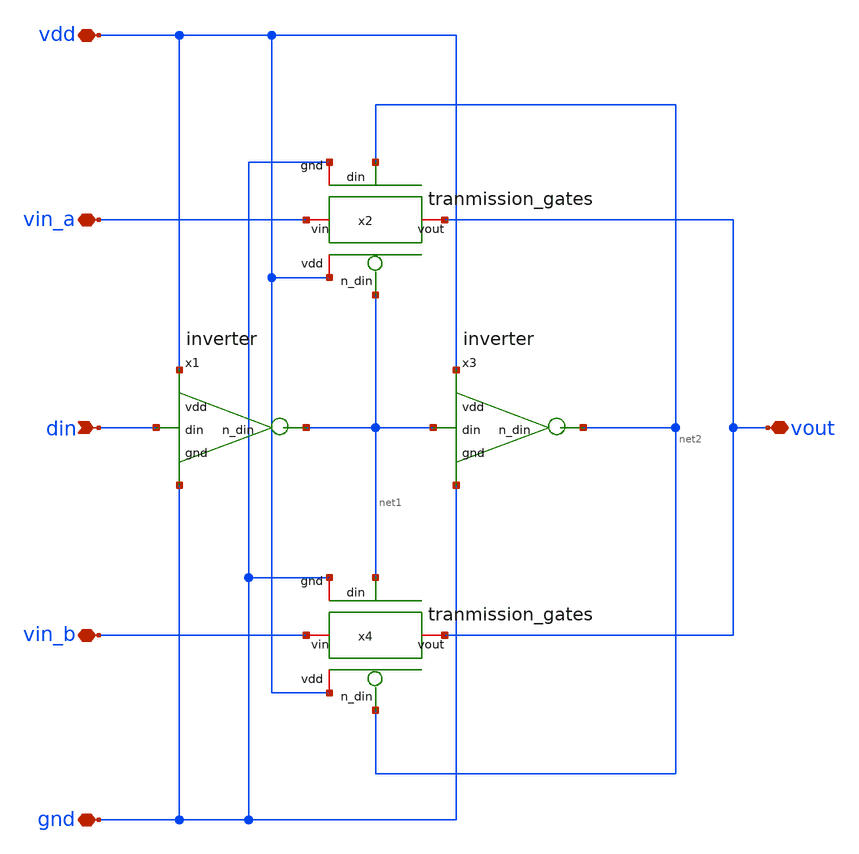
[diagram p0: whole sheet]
** sch_path: Symbols/spdt_sw.sch
**.subckt spdt_sw vdd gnd vout vin_a vin_b din
*.iopin vdd
*.iopin gnd
*.iopin vout
*.iopin vin_a
*.iopin vin_b
*.ipin din
x1 vdd din net1 gnd inverter
x2 net1 vdd vout vin_a gnd net2 tranmission_gates
x3 vdd net1 net2 gnd inverter
x4 net2 vdd vout vin_b gnd net1 tranmission_gates
**.ends

* expanding   symbol:  inverter.sym # of pins=4
** sym_path: Symbols/inverter.sym
** sch_path: Symbols/inverter.sch
.subckt inverter vdd din n_din gnd
*.ipin gnd
*.opin n_din
*.ipin din
*.ipin vdd
XM3 n_din din vdd vdd sky130_fd_pr__pfet_01v8 L=1 W=1 nf=1 ad='int((nf+1)/2) * W/nf * 0.29' as='int((nf+2)/2) * W/nf * 0.29'
+ pd='2*int((nf+1)/2) * (W/nf + 0.29)' ps='2*int((nf+2)/2) * (W/nf + 0.29)' nrd='0.29 / W' nrs='0.29 / W'
+ sa=0 sb=0 sd=0 mult=1 m=1
XM4 n_din din gnd gnd sky130_fd_pr__nfet_01v8 L=1 W=1 nf=1 ad='int((1 + 1)/2) * 1 / 1 * 0.29' as='int((1 + 2)/2) * 1 / 1 * 0.29'
+ pd='2*int((1 + 1)/2) * (1 / 1 + 0.29)' ps='2*int((1 + 2)/2) * (1 / 1 + 0.29)' nrd='0.29 / 1 ' nrs='0.29 / 1 '
+ sa=0 sb=0 sd=0 mult=1 m=1
.ends


* expanding   symbol:  tranmission_gates.sym # of pins=6
** sym_path: Symbols/tranmission_gates.sym
** sch_path: Symbols/tranmission_gates.sch
.subckt tranmission_gates n_din vdd vout vin gnd din
*.ipin din
*.ipin n_din
*.iopin vdd
*.iopin gnd
*.iopin vin
*.iopin vout
XM3 vout n_din vin vdd sky130_fd_pr__pfet_01v8 L=1 W=10 nf=1 ad='int((nf+1)/2) * W/nf * 0.29' as='int((nf+2)/2) * W/nf * 0.29'
+ pd='2*int((nf+1)/2) * (W/nf + 0.29)' ps='2*int((nf+2)/2) * (W/nf + 0.29)' nrd='0.29 / W' nrs='0.29 / W'
+ sa=0 sb=0 sd=0 mult=1 m=1
XM4 vin din vout gnd sky130_fd_pr__nfet_01v8 L=1 W=1 nf=1 ad='int((1 + 1)/2) * 1 / 1 * 0.29' as='int((1 + 2)/2) * 1 / 1 * 0.29'
+ pd='2*int((1 + 1)/2) * (1 / 1 + 0.29)' ps='2*int((1 + 2)/2) * (1 / 1 + 0.29)' nrd='0.29 / 1 ' nrs='0.29 / 1 '
+ sa=0 sb=0 sd=0 mult=1 m=1
.ends

.end
